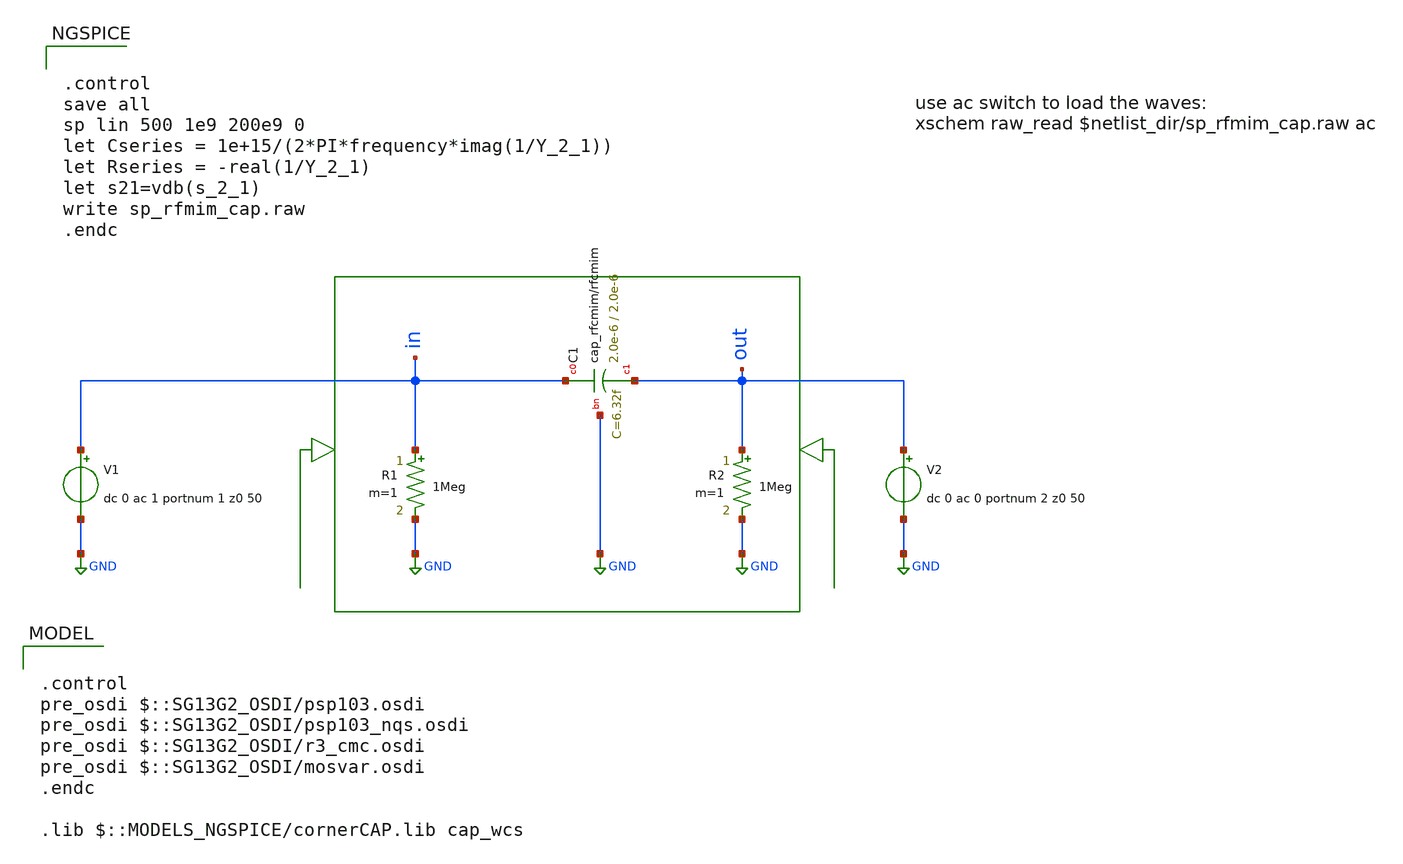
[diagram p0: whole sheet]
** sch_path: ihp-sg13g2/xschem_libs/sg13g2_tests/sp_rfmim_cap/schematic/sp_rfmim_cap.sch
* Copyright 2021 Stefan Frederik Schippers
* Licensed under the Apache License, Version 2.0 (the "License");
* you may not use this file except in compliance with the License.
* You may obtain a copy of the License at
* https://www.apache.org/licenses/LICENSE-2.0
* Unless required by applicable law or agreed to in writing, software
* distributed under the License is distributed on an "AS IS" BASIS,
* WITHOUT WARRANTIES OR CONDITIONS OF ANY KIND, either express or implied.
* See the License for the specific language governing permissions and
* limitations under the License.
* Copyright 2023 IHP PDK Authors
**.subckt sp_rfmim_cap
R1 in GND 1Meg m=1
V1 in GND dc 0 ac 1 portnum 1 z0 50
R2 out GND 1Meg m=1
V2 out GND dc 0 ac 0 portnum 2 z0 50
XC1 in out GND cap_rfcmim w=2.0e-6 l=2.0e-6 wfeed=5.0e-6 m=1 mm_ok=1
**** begin user architecture code


.control
save all
sp lin 500 1e9 200e9 0
let Cseries = 1e+15/(2*PI*frequency*imag(1/Y_2_1))
let Rseries = -real(1/Y_2_1)
let s21=vdb(s_2_1)
write sp_rfmim_cap.raw
.endc



.control
pre_osdi $::SG13G2_OSDI/psp103.osdi
pre_osdi $::SG13G2_OSDI/psp103_nqs.osdi
pre_osdi $::SG13G2_OSDI/r3_cmc.osdi
pre_osdi $::SG13G2_OSDI/mosvar.osdi
.endc

.lib $::MODELS_NGSPICE/cornerCAP.lib cap_wcs

**** end user architecture code
**.ends
.GLOBAL GND
.end
